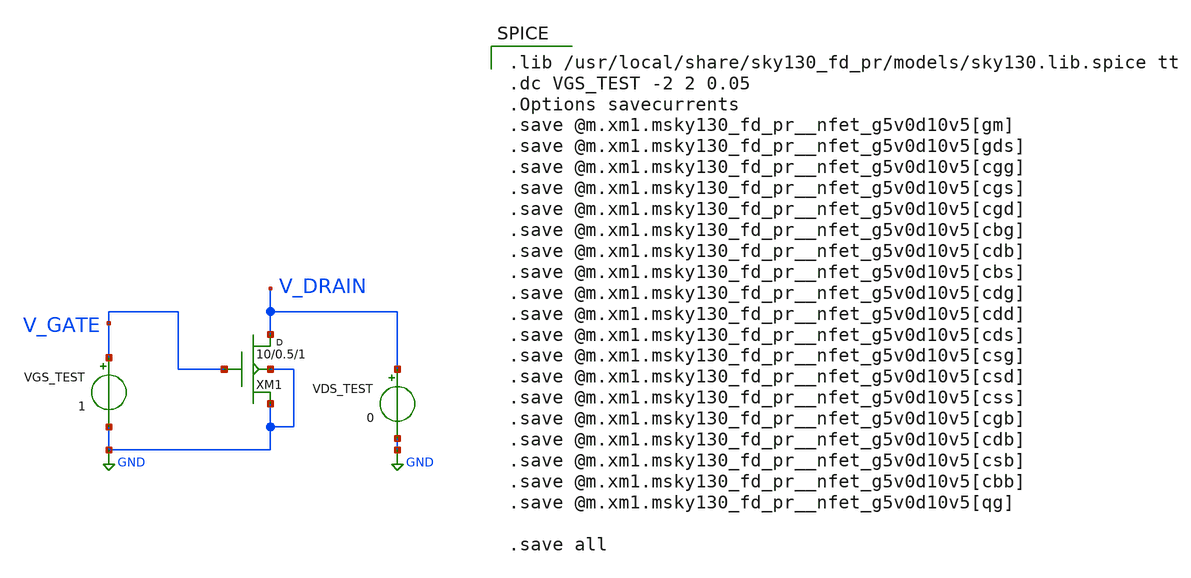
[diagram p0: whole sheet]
** sch_path: images/foss-asic-tools/addons/examples/sky130-analog/device/sims/Pfet_sweep_gate.sch
**.subckt Pfet_sweep_gate
VGS_TEST V_GATE GND 1
XM1 V_DRAIN V_GATE GND GND sky130_fd_pr__nfet_g5v0d10v5 w=10 l=0.5 m=1
VDS_TEST V_DRAIN GND 0
**** begin user architecture code

.lib /usr/local/share/sky130_fd_pr/models/sky130.lib.spice tt
.dc VGS_TEST -2 2 0.05
.Options savecurrents
.save @m.xm1.msky130_fd_pr__nfet_g5v0d10v5[gm]
.save @m.xm1.msky130_fd_pr__nfet_g5v0d10v5[gds]
.save @m.xm1.msky130_fd_pr__nfet_g5v0d10v5[cgg]
.save @m.xm1.msky130_fd_pr__nfet_g5v0d10v5[cgs]
.save @m.xm1.msky130_fd_pr__nfet_g5v0d10v5[cgd]
.save @m.xm1.msky130_fd_pr__nfet_g5v0d10v5[cbg]
.save @m.xm1.msky130_fd_pr__nfet_g5v0d10v5[cdb]
.save @m.xm1.msky130_fd_pr__nfet_g5v0d10v5[cbs]
.save @m.xm1.msky130_fd_pr__nfet_g5v0d10v5[cdg]
.save @m.xm1.msky130_fd_pr__nfet_g5v0d10v5[cdd]
.save @m.xm1.msky130_fd_pr__nfet_g5v0d10v5[cds]
.save @m.xm1.msky130_fd_pr__nfet_g5v0d10v5[csg]
.save @m.xm1.msky130_fd_pr__nfet_g5v0d10v5[csd]
.save @m.xm1.msky130_fd_pr__nfet_g5v0d10v5[css]
.save @m.xm1.msky130_fd_pr__nfet_g5v0d10v5[cgb]
.save @m.xm1.msky130_fd_pr__nfet_g5v0d10v5[cdb]
.save @m.xm1.msky130_fd_pr__nfet_g5v0d10v5[csb]
.save @m.xm1.msky130_fd_pr__nfet_g5v0d10v5[cbb]
.save @m.xm1.msky130_fd_pr__nfet_g5v0d10v5[qg]

.save all

**** end user architecture code
**.ends
.GLOBAL GND
.end
